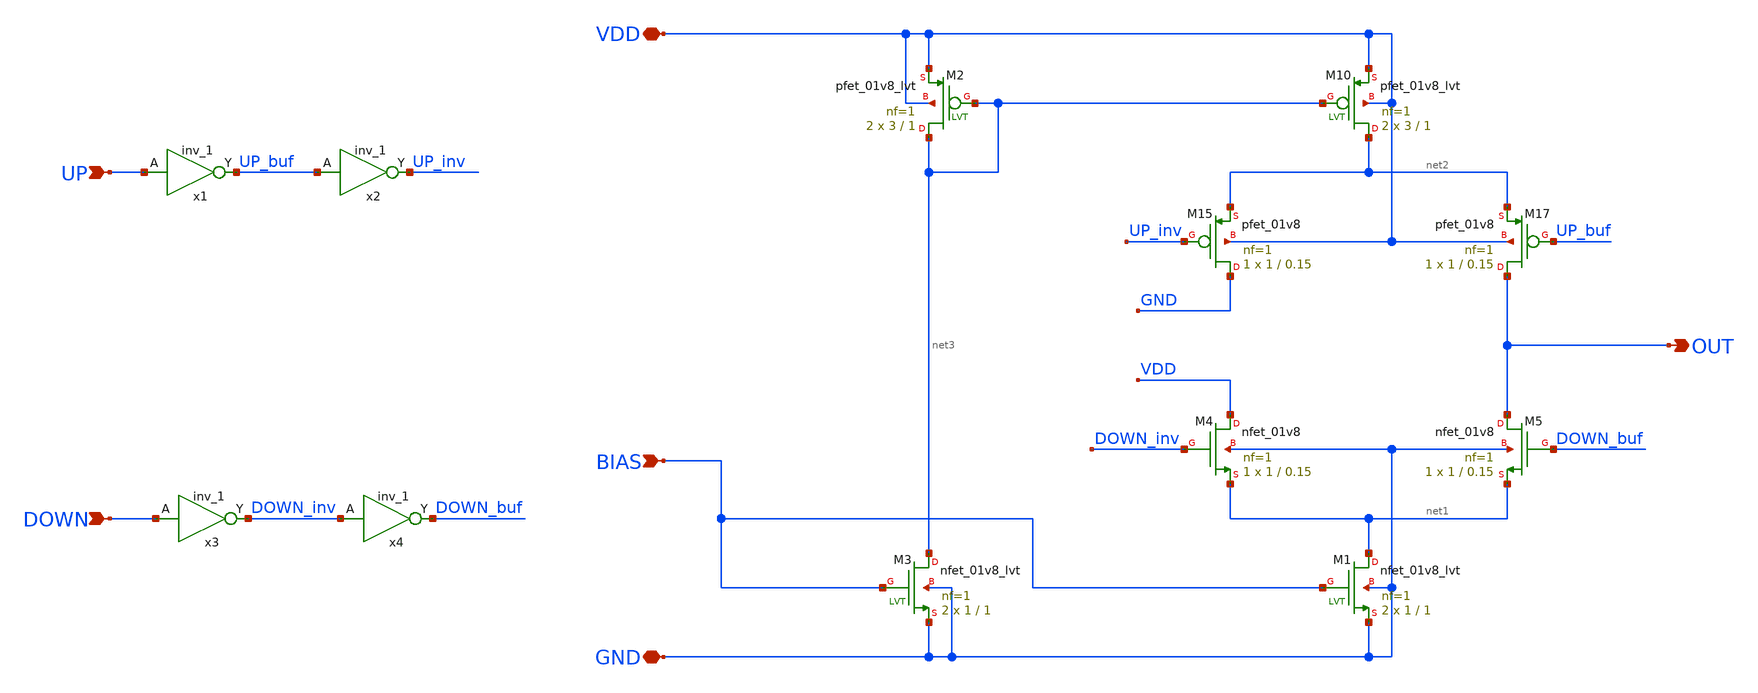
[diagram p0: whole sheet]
** sch_path: xschem/chargepump/chargepump.sch
**.subckt chargepump BIAS OUT UP DOWN VDD GND
*.ipin BIAS
*.opin OUT
*.ipin UP
*.ipin DOWN
*.iopin VDD
*.iopin GND
XM2 net3 net3 VDD VDD sky130_fd_pr__pfet_01v8_lvt L=1 W=3 nf=1 ad='W * 0.29' as='W * 0.29' pd='2 * (W + 0.29)'
+ ps='2 * (W + 0.29)' nrd='0.29 / W' nrs='0.29 / W' sa=0 sb=0 sd=0 mult=2 m=2
XM10 net2 net3 VDD VDD sky130_fd_pr__pfet_01v8_lvt L=1 W=3 nf=1 ad='W * 0.29' as='W * 0.29' pd='2 * (W + 0.29)'
+ ps='2 * (W + 0.29)' nrd='0.29 / W' nrs='0.29 / W' sa=0 sb=0 sd=0 mult=2 m=2
XM15 GND UP_inv net2 VDD sky130_fd_pr__pfet_01v8 L=0.15 W=1 nf=1 ad='W * 0.29' as='W * 0.29' pd='2 * (W + 0.29)'
+ ps='2 * (W + 0.29)' nrd='0.29 / W' nrs='0.29 / W' sa=0 sb=0 sd=0 mult=1 m=1
XM17 OUT UP_buf net2 VDD sky130_fd_pr__pfet_01v8 L=0.15 W=1 nf=1 ad='W * 0.29' as='W * 0.29' pd='2 * (W + 0.29)'
+ ps='2 * (W + 0.29)' nrd='0.29 / W' nrs='0.29 / W' sa=0 sb=0 sd=0 mult=1 m=1
x1 UP gnd gnd vdd vdd UP_buf sky130_fd_sc_hd__inv_1
x2 UP_buf gnd gnd vdd vdd UP_inv sky130_fd_sc_hd__inv_1
x3 DOWN gnd gnd vdd vdd DOWN_inv sky130_fd_sc_hd__inv_1
x4 DOWN_inv gnd gnd vdd vdd DOWN_buf sky130_fd_sc_hd__inv_1
XM1 net1 BIAS GND GND sky130_fd_pr__nfet_01v8_lvt L=1 W=1 nf=1 ad='W * 0.29' as='W * 0.29' pd='2 * (W + 0.29)'
+ ps='2 * (W + 0.29)' nrd='0.29 / W' nrs='0.29 / W' sa=0 sb=0 sd=0 mult=2 m=2
XM3 net3 BIAS GND GND sky130_fd_pr__nfet_01v8_lvt L=1 W=1 nf=1 ad='W * 0.29' as='W * 0.29' pd='2 * (W + 0.29)'
+ ps='2 * (W + 0.29)' nrd='0.29 / W' nrs='0.29 / W' sa=0 sb=0 sd=0 mult=2 m=2
XM4 VDD DOWN_inv net1 GND sky130_fd_pr__nfet_01v8 L=0.15 W=1 nf=1 ad='W * 0.29' as='W * 0.29' pd='2 * (W + 0.29)'
+ ps='2 * (W + 0.29)' nrd='0.29 / W' nrs='0.29 / W' sa=0 sb=0 sd=0 mult=1 m=1
XM5 OUT DOWN_buf net1 GND sky130_fd_pr__nfet_01v8 L=0.15 W=1 nf=1 ad='W * 0.29' as='W * 0.29' pd='2 * (W + 0.29)'
+ ps='2 * (W + 0.29)' nrd='0.29 / W' nrs='0.29 / W' sa=0 sb=0 sd=0 mult=1 m=1
**.ends
.end
